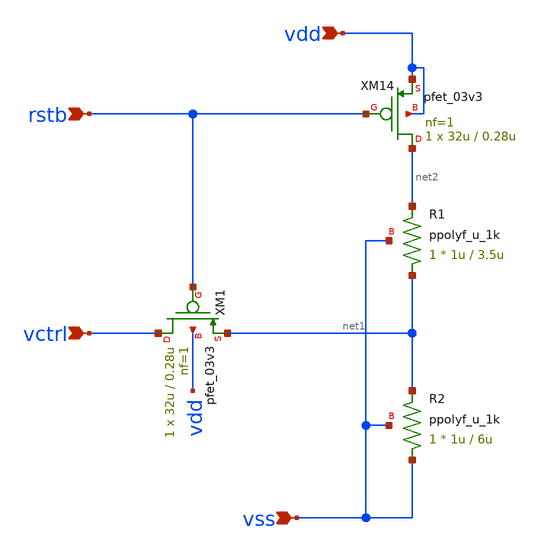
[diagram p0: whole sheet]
** sch_path: xschem/vctrl_startup.sch
**.subckt vctrl_startup vdd rstb vctrl vss
*.ipin vdd
*.ipin rstb
*.ipin vctrl
*.ipin vss
XM14 net2 rstb vdd vdd pfet_03v3 L=0.28u W=32u nf=1 ad='int((nf+1)/2) * W/nf * 0.18u' as='int((nf+2)/2) * W/nf * 0.18u'
+ pd='2*int((nf+1)/2) * (W/nf + 0.18u)' ps='2*int((nf+2)/2) * (W/nf + 0.18u)' nrd='0.18u / W' nrs='0.18u / W'
+ sa=0 sb=0 sd=0 m=1
XM1 vctrl rstb net1 vdd pfet_03v3 L=0.28u W=32u nf=1 ad='int((nf+1)/2) * W/nf * 0.18u' as='int((nf+2)/2) * W/nf * 0.18u'
+ pd='2*int((nf+1)/2) * (W/nf + 0.18u)' ps='2*int((nf+2)/2) * (W/nf + 0.18u)' nrd='0.18u / W' nrs='0.18u / W'
+ sa=0 sb=0 sd=0 m=1
XR1 net1 net2 vss ppolyf_u_1k r_width=1u r_length=3.5u m=1
XR2 vss net1 vss ppolyf_u_1k r_width=1u r_length=6u m=1
**.ends
.end
